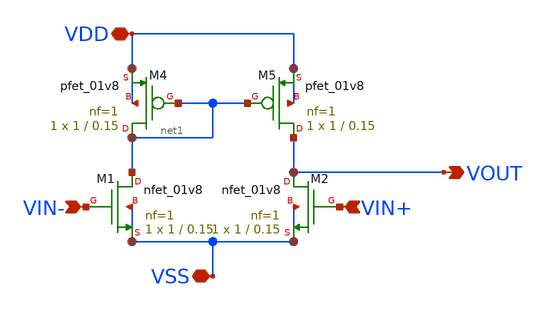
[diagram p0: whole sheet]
** sch_path: analog/bootcamp_opamp/schematics/opamp_single_stage.sch
**.subckt opamp_single_stage VIN- VSS VIN+ VOUT VDD
*.ipin VIN-
*.iopin VSS
*.ipin VIN+
*.opin VOUT
*.iopin VDD
XM1 net1 VIN- VSS VSS sky130_fd_pr__nfet_01v8 L=0.15 W=1 nf=1 ad='int((nf+1)/2) * W/nf * 0.29' as='int((nf+2)/2) * W/nf * 0.29'
+ pd='2*int((nf+1)/2) * (W/nf + 0.29)' ps='2*int((nf+2)/2) * (W/nf + 0.29)' nrd='0.29 / W' nrs='0.29 / W'
+ sa=0 sb=0 sd=0 mult=1 m=1
XM2 VOUT VIN+ VSS VSS sky130_fd_pr__nfet_01v8 L=0.15 W=1 nf=1 ad='int((nf+1)/2) * W/nf * 0.29' as='int((nf+2)/2) * W/nf * 0.29'
+ pd='2*int((nf+1)/2) * (W/nf + 0.29)' ps='2*int((nf+2)/2) * (W/nf + 0.29)' nrd='0.29 / W' nrs='0.29 / W'
+ sa=0 sb=0 sd=0 mult=1 m=1
XM4 net1 net1 VDD VDD sky130_fd_pr__pfet_01v8 L=0.15 W=1 nf=1 ad='int((nf+1)/2) * W/nf * 0.29' as='int((nf+2)/2) * W/nf * 0.29'
+ pd='2*int((nf+1)/2) * (W/nf + 0.29)' ps='2*int((nf+2)/2) * (W/nf + 0.29)' nrd='0.29 / W' nrs='0.29 / W'
+ sa=0 sb=0 sd=0 mult=1 m=1
XM5 VOUT net1 VDD VDD sky130_fd_pr__pfet_01v8 L=0.15 W=1 nf=1 ad='int((nf+1)/2) * W/nf * 0.29' as='int((nf+2)/2) * W/nf * 0.29'
+ pd='2*int((nf+1)/2) * (W/nf + 0.29)' ps='2*int((nf+2)/2) * (W/nf + 0.29)' nrd='0.29 / W' nrs='0.29 / W'
+ sa=0 sb=0 sd=0 mult=1 m=1
**.ends
.end
